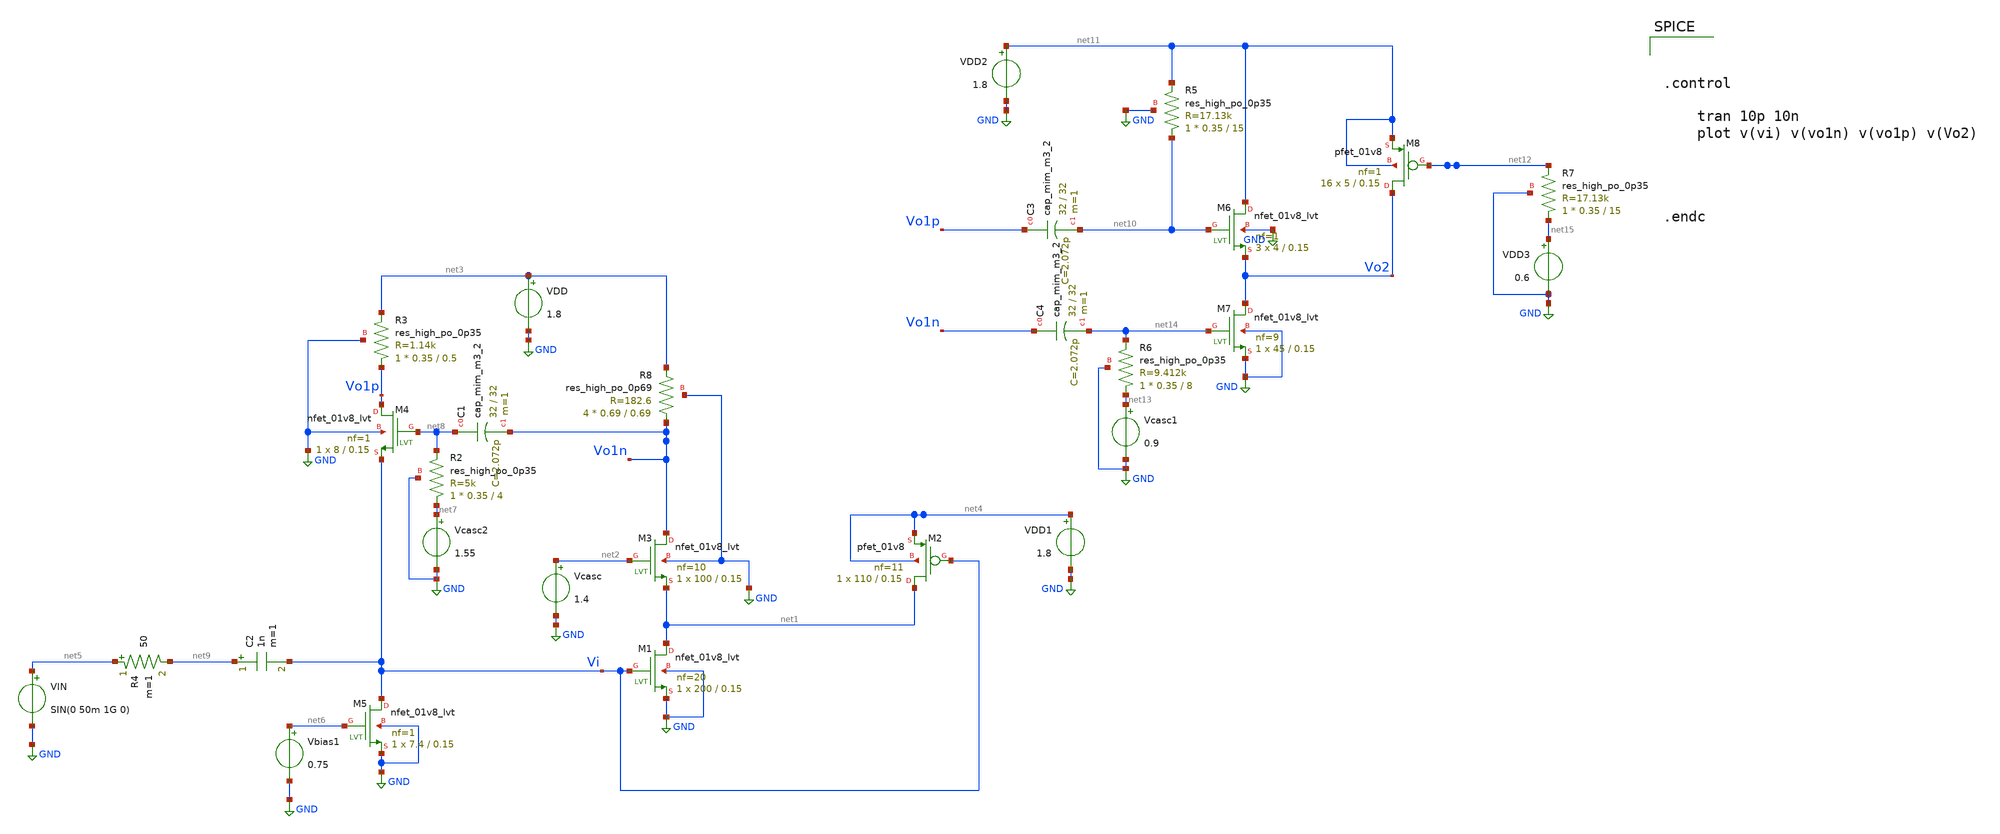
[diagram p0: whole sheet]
** sch_path: xschem/LNA_TRANS.sch
**.subckt LNA_TRANS
VIN net5 GND SIN(0 50m 1G 0)
Vcasc net2 GND 1.4
VDD net3 GND 1.8
VDD1 net4 GND 1.8
Vbias1 net6 GND 0.75
Vcasc2 net7 GND 1.55
XR2 net7 net8 GND sky130_fd_pr__res_high_po_0p35 L=4 mult=1 m=1
XC1 net8 Vo1n sky130_fd_pr__cap_mim_m3_2 W=32 L=32 MF=1 m=1
C2 net9 Vi 1n m=1
XM1 net1 Vi GND GND sky130_fd_pr__nfet_01v8_lvt L=0.15 W=200 nf=20 ad='int((nf+1)/2) * W/nf * 0.29' as='int((nf+2)/2) * W/nf * 0.29'
+ pd='2*int((nf+1)/2) * (W/nf + 0.29)' ps='2*int((nf+2)/2) * (W/nf + 0.29)' nrd='0.29 / W' nrs='0.29 / W'
+ sa=0 sb=0 sd=0 mult=1 m=1
XM2 net1 Vi net4 net4 sky130_fd_pr__pfet_01v8 L=0.15 W=110 nf=11 ad='int((nf+1)/2) * W/nf * 0.29' as='int((nf+2)/2) * W/nf * 0.29'
+ pd='2*int((nf+1)/2) * (W/nf + 0.29)' ps='2*int((nf+2)/2) * (W/nf + 0.29)' nrd='0.29 / W' nrs='0.29 / W'
+ sa=0 sb=0 sd=0 mult=1 m=1
XM3 Vo1n net2 net1 GND sky130_fd_pr__nfet_01v8_lvt L=0.15 W=100 nf=10 ad='int((nf+1)/2) * W/nf * 0.29'
+ as='int((nf+2)/2) * W/nf * 0.29' pd='2*int((nf+1)/2) * (W/nf + 0.29)' ps='2*int((nf+2)/2) * (W/nf + 0.29)'
+ nrd='0.29 / W' nrs='0.29 / W' sa=0 sb=0 sd=0 mult=1 m=1
XM4 Vo1p net8 Vi GND sky130_fd_pr__nfet_01v8_lvt L=0.15 W=8 nf=1 ad='int((nf+1)/2) * W/nf * 0.29' as='int((nf+2)/2) * W/nf * 0.29'
+ pd='2*int((nf+1)/2) * (W/nf + 0.29)' ps='2*int((nf+2)/2) * (W/nf + 0.29)' nrd='0.29 / W' nrs='0.29 / W'
+ sa=0 sb=0 sd=0 mult=1 m=1
XM5 Vi net6 GND GND sky130_fd_pr__nfet_01v8_lvt L=0.15 W=7.4 nf=1 ad='int((nf+1)/2) * W/nf * 0.29' as='int((nf+2)/2) * W/nf * 0.29'
+ pd='2*int((nf+1)/2) * (W/nf + 0.29)' ps='2*int((nf+2)/2) * (W/nf + 0.29)' nrd='0.29 / W' nrs='0.29 / W'
+ sa=0 sb=0 sd=0 mult=1 m=1
R4 net5 net9 50 m=1
XM7 Vo2 net14 GND GND sky130_fd_pr__nfet_01v8_lvt L=0.15 W=45 nf=9 ad='int((nf+1)/2) * W/nf * 0.29' as='int((nf+2)/2) * W/nf * 0.29'
+ pd='2*int((nf+1)/2) * (W/nf + 0.29)' ps='2*int((nf+2)/2) * (W/nf + 0.29)' nrd='0.29 / W' nrs='0.29 / W'
+ sa=0 sb=0 sd=0 mult=1 m=1
XM6 net11 net10 Vo2 GND sky130_fd_pr__nfet_01v8_lvt L=0.15 W=4 nf=1 ad='int((nf+1)/2) * W/nf * 0.29'
+ as='int((nf+2)/2) * W/nf * 0.29' pd='2*int((nf+1)/2) * (W/nf + 0.29)' ps='2*int((nf+2)/2) * (W/nf + 0.29)'
+ nrd='0.29 / W' nrs='0.29 / W' sa=0 sb=0 sd=0 mult=3 m=3
XR5 net10 net11 GND sky130_fd_pr__res_high_po_0p35 L=15 mult=1 m=1
XM8 Vo2 net12 net11 net11 sky130_fd_pr__pfet_01v8 L=0.15 W=5 nf=1 ad='int((nf+1)/2) * W/nf * 0.29' as='int((nf+2)/2) * W/nf * 0.29'
+ pd='2*int((nf+1)/2) * (W/nf + 0.29)' ps='2*int((nf+2)/2) * (W/nf + 0.29)' nrd='0.29 / W' nrs='0.29 / W'
+ sa=0 sb=0 sd=0 mult=16 m=16
VDD2 net11 GND 1.8
VDD3 net15 GND 0.6
XC3 Vo1p net10 sky130_fd_pr__cap_mim_m3_2 W=32 L=32 MF=1 m=1
Vcasc1 net13 GND 0.9
XR6 net13 net14 GND sky130_fd_pr__res_high_po_0p35 L=8 mult=1 m=1
XC4 Vo1n net14 sky130_fd_pr__cap_mim_m3_2 W=32 L=32 MF=1 m=1
XR7 net15 net12 GND sky130_fd_pr__res_high_po_0p35 L=15 mult=1 m=1
XR8 Vo1n net3 GND sky130_fd_pr__res_high_po_0p69 L=0.69 mult=4 m=4
XR3 Vo1p net3 GND sky130_fd_pr__res_high_po_0p35 L=0.5 mult=1 m=1
**** begin user architecture code

.lib $::SKYWATER_MODELS/sky130.lib.spice tt




.control

	tran 10p 10n
	plot v(vi) v(vo1n) v(vo1p) v(Vo2)




.endc


**** end user architecture code
**.ends
.GLOBAL GND
.end
